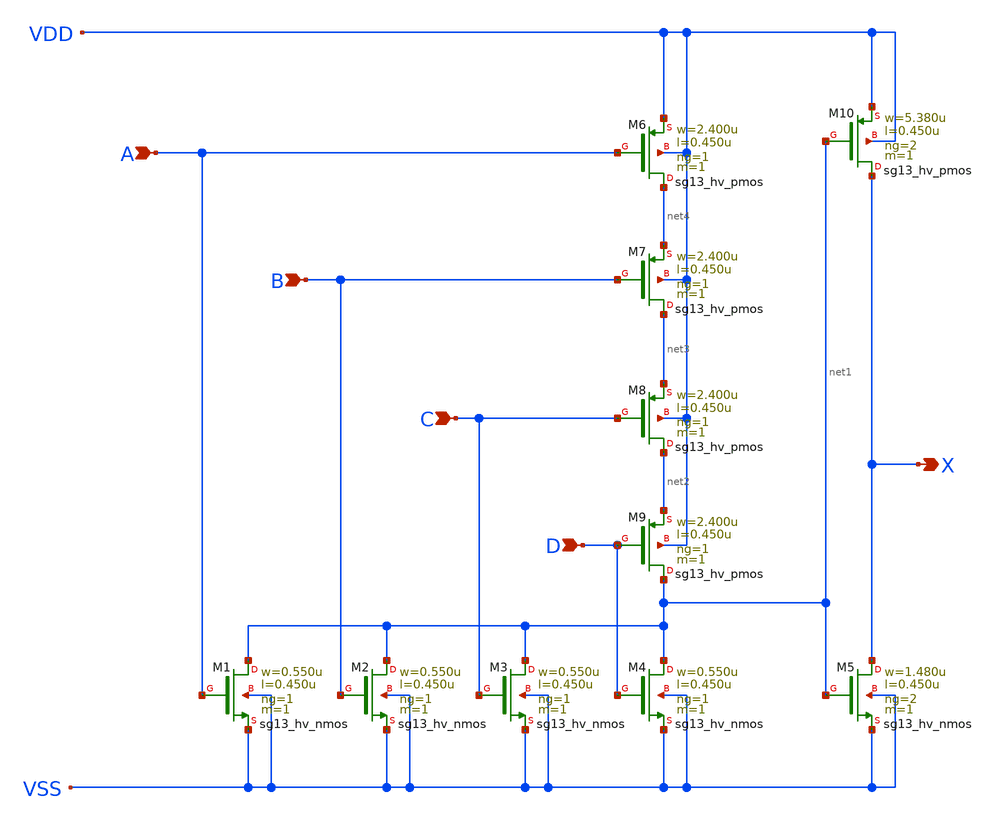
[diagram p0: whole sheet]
** sch_path: ihp-sg13g2/libs.ref/sg13g2_stdcell_hv/sch/xschem/sg13g2_hv_or4_2.sch
* Copyright 2023 IHP PDK Authors
* Licensed under the Apache License, Version 2.0 (the "License");
* you may not use this file except in compliance with the License.
* You may obtain a copy of the License at
* https://www.apache.org/licenses/LICENSE-2.0
* Unless required by applicable law or agreed to in writing, software
* distributed under the License is distributed on an "AS IS" BASIS,
* WITHOUT WARRANTIES OR CONDITIONS OF ANY KIND, either express or implied.
* See the License for the specific language governing permissions and
* limitations under the License.
**.subckt sg13g2_hv_or4_2 X A B C D
*.opin X
*.ipin A
*.ipin B
*.ipin C
*.ipin D
XM1 net1 A VSS VSS sg13_hv_nmos w=0.550u l=0.450u ng=1 m=1 mm_ok=1
XM2 net1 B VSS VSS sg13_hv_nmos w=0.550u l=0.450u ng=1 m=1 mm_ok=1
XM3 net1 C VSS VSS sg13_hv_nmos w=0.550u l=0.450u ng=1 m=1 mm_ok=1
XM4 net1 D VSS VSS sg13_hv_nmos w=0.550u l=0.450u ng=1 m=1 mm_ok=1
XM5 X net1 VSS VSS sg13_hv_nmos w=1.480u l=0.450u ng=2 m=1 mm_ok=1
XM6 net4 A VDD VDD sg13_hv_pmos w=2.400u l=0.450u ng=1 m=1 mm_ok=1
XM7 net3 B net4 VDD sg13_hv_pmos w=2.400u l=0.450u ng=1 m=1 mm_ok=1
XM8 net2 C net3 VDD sg13_hv_pmos w=2.400u l=0.450u ng=1 m=1 mm_ok=1
XM9 net1 D net2 VDD sg13_hv_pmos w=2.400u l=0.450u ng=1 m=1 mm_ok=1
XM10 X net1 VDD VDD sg13_hv_pmos w=5.380u l=0.450u ng=2 m=1 mm_ok=1
**.ends
.end
